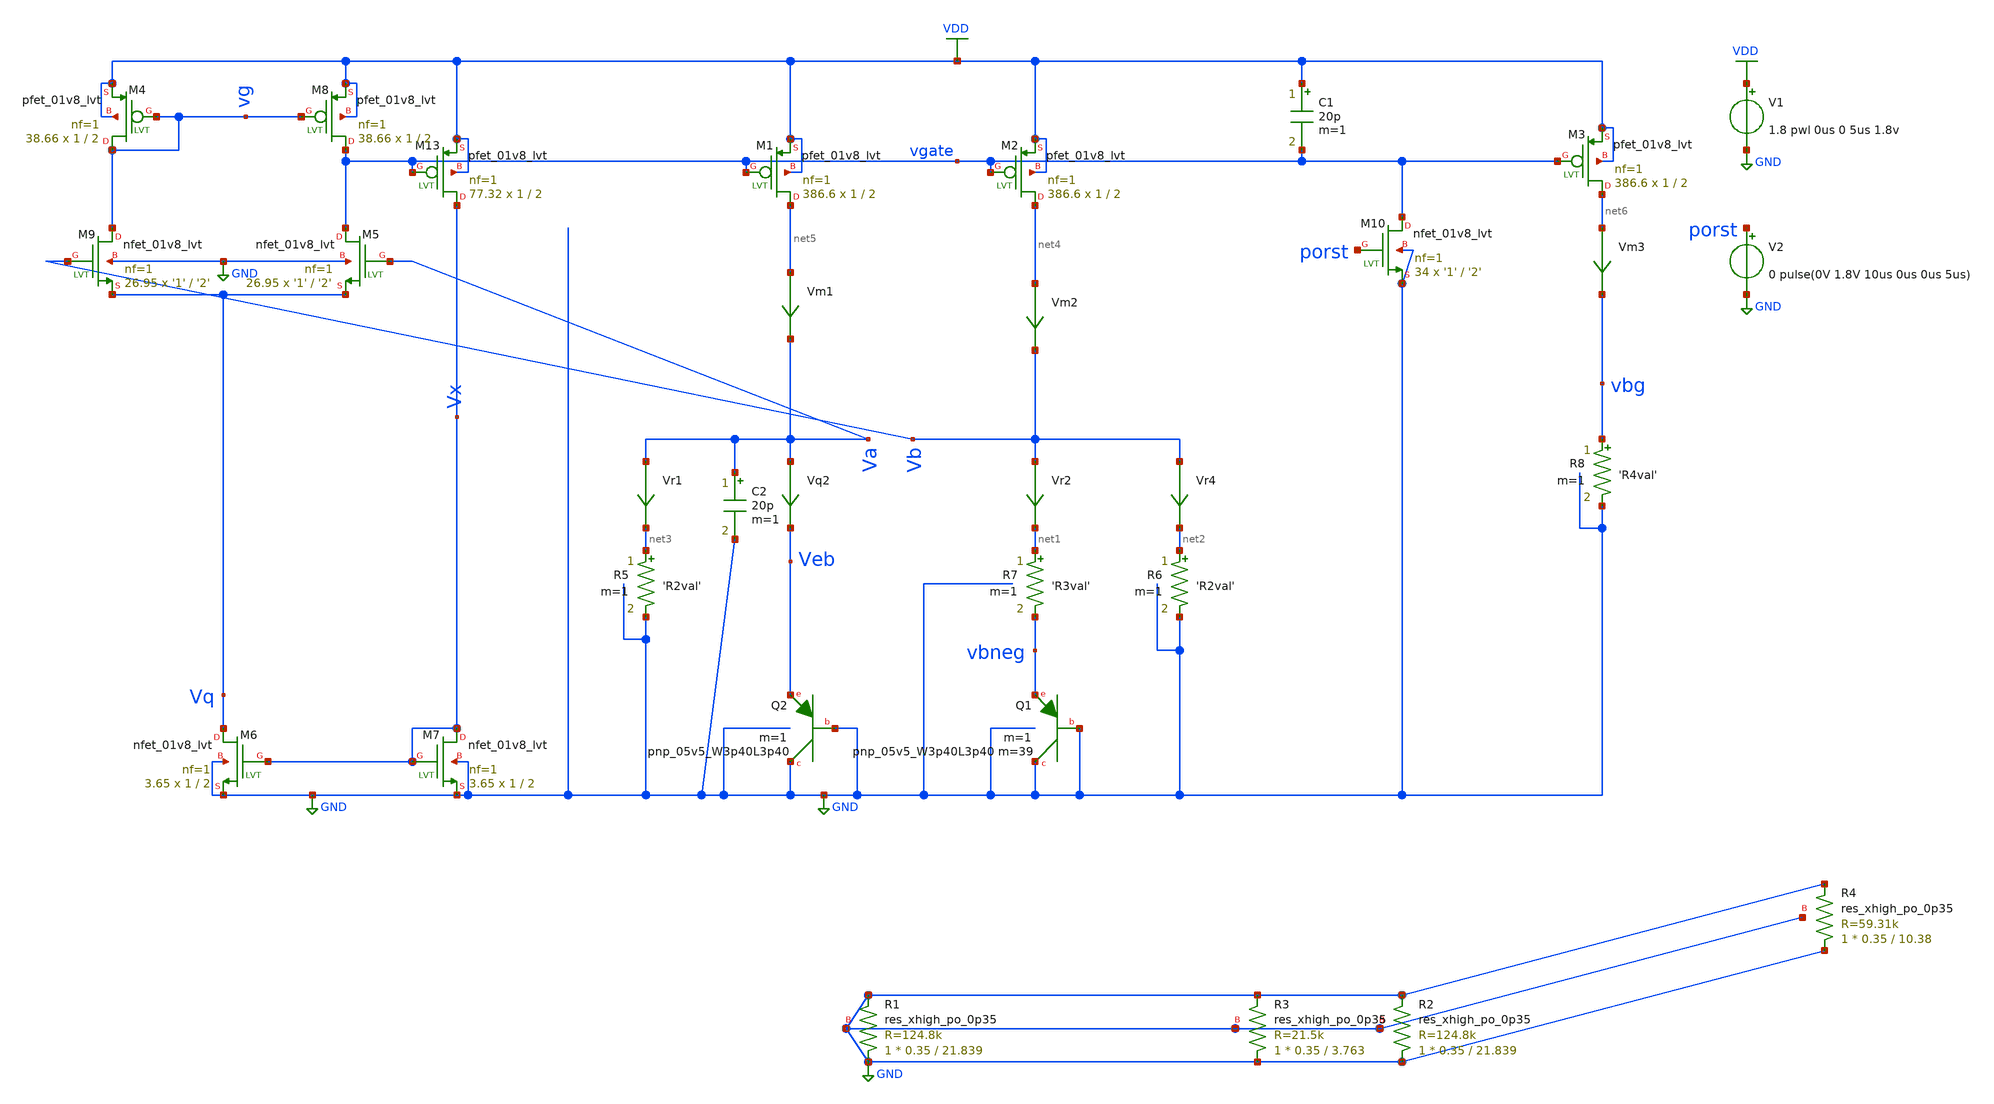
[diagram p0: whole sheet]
** sch_path: schematics/tsmc_bandgap_real.sch
**.subckt tsmc_bandgap_real
V1 VDD GND 1.8 pwl 0us 0 5us 1.8v
XQ2 GND GND Veb sky130_fd_pr__pnp_05v5_W3p40L3p40 m=1
Vr4 Vb net2 0
.save i(vr4)
Vr2 Vb net1 0
.save i(vr2)
Vm1 net5 Va 0
.save i(vm1)
Vm2 net4 Vb 0
.save i(vm2)
Vm3 net6 vbg 0
.save i(vm3)
Vr1 Va net3 0
.save i(vr1)
Vq2 Va Veb 0
.save i(vq2)
XQ1 GND GND vbneg sky130_fd_pr__pnp_05v5_W3p40L3p40 m=39 m=1
XM5 vgate Va Vq GND sky130_fd_pr__nfet_01v8_lvt L='2' W='1' nf=1 ad='int((nf+1)/2) * W/nf * 0.29' as='int((nf+2)/2) * W/nf * 0.29'
+ pd='2*int((nf+1)/2) * (W/nf + 0.29)' ps='2*int((nf+2)/2) * (W/nf + 0.29)' nrd='0.29 / W' nrs='0.29 / W'
+ sa=0 sb=0 sd=0 mult=26.95 m=26.95
XM6 Vq Vx GND GND sky130_fd_pr__nfet_01v8_lvt L=2 W=1 nf=1 ad='int((nf+1)/2) * W/nf * 0.29' as='int((nf+2)/2) * W/nf * 0.29'
+ pd='2*int((nf+1)/2) * (W/nf + 0.29)' ps='2*int((nf+2)/2) * (W/nf + 0.29)' nrd='0.29 / W' nrs='0.29 / W'
+ sa=0 sb=0 sd=0 mult=3.65 m=3.65
XM9 vg Vb Vq GND sky130_fd_pr__nfet_01v8_lvt L='2' W='1' nf=1 ad='int((nf+1)/2) * W/nf * 0.29' as='int((nf+2)/2) * W/nf * 0.29'
+ pd='2*int((nf+1)/2) * (W/nf + 0.29)' ps='2*int((nf+2)/2) * (W/nf + 0.29)' nrd='0.29 / W' nrs='0.29 / W'
+ sa=0 sb=0 sd=0 mult=26.95 m=26.95
XM7 Vx Vx GND GND sky130_fd_pr__nfet_01v8_lvt L=2 W=1 nf=1 ad='int((nf+1)/2) * W/nf * 0.29' as='int((nf+2)/2) * W/nf * 0.29'
+ pd='2*int((nf+1)/2) * (W/nf + 0.29)' ps='2*int((nf+2)/2) * (W/nf + 0.29)' nrd='0.29 / W' nrs='0.29 / W'
+ sa=0 sb=0 sd=0 mult=3.65 m=3.65
XM13 Vx vgate VDD VDD sky130_fd_pr__pfet_01v8_lvt L=2 W=1 nf=1 ad='int((nf+1)/2) * W/nf * 0.29' as='int((nf+2)/2) * W/nf * 0.29'
+ pd='2*int((nf+1)/2) * (W/nf + 0.29)' ps='2*int((nf+2)/2) * (W/nf + 0.29)' nrd='0.29 / W' nrs='0.29 / W'
+ sa=0 sb=0 sd=0 mult=77.32 m=77.32
XM1 net5 vgate VDD VDD sky130_fd_pr__pfet_01v8_lvt L=2 W=1 nf=1 ad='int((nf+1)/2) * W/nf * 0.29' as='int((nf+2)/2) * W/nf * 0.29'
+ pd='2*int((nf+1)/2) * (W/nf + 0.29)' ps='2*int((nf+2)/2) * (W/nf + 0.29)' nrd='0.29 / W' nrs='0.29 / W'
+ sa=0 sb=0 sd=0 mult=386.6 m=386.6
XM2 net4 vgate VDD VDD sky130_fd_pr__pfet_01v8_lvt L=2 W=1 nf=1 ad='int((nf+1)/2) * W/nf * 0.29' as='int((nf+2)/2) * W/nf * 0.29'
+ pd='2*int((nf+1)/2) * (W/nf + 0.29)' ps='2*int((nf+2)/2) * (W/nf + 0.29)' nrd='0.29 / W' nrs='0.29 / W'
+ sa=0 sb=0 sd=0 mult=386.6 m=386.6
XM3 net6 vgate VDD VDD sky130_fd_pr__pfet_01v8_lvt L=2 W=1 nf=1 ad='int((nf+1)/2) * W/nf * 0.29' as='int((nf+2)/2) * W/nf * 0.29'
+ pd='2*int((nf+1)/2) * (W/nf + 0.29)' ps='2*int((nf+2)/2) * (W/nf + 0.29)' nrd='0.29 / W' nrs='0.29 / W'
+ sa=0 sb=0 sd=0 mult=386.6 m=386.6
XR1 GND GND GND sky130_fd_pr__res_xhigh_po_0p35 L=21.839 mult=1 m=1
XR2 GND GND GND sky130_fd_pr__res_xhigh_po_0p35 L=21.839 mult=1 m=1
XR3 GND GND GND sky130_fd_pr__res_xhigh_po_0p35 L=3.763 mult=1 m=1
XR4 GND GND GND sky130_fd_pr__res_xhigh_po_0p35 L=10.38 mult=1 m=1
R7 net1 vbneg 'R3val' m=1
R5 net3 GND 'R2val' m=1
R6 net2 GND 'R2val' m=1
R8 vbg GND 'R4val' m=1
XM4 vg vg VDD VDD sky130_fd_pr__pfet_01v8_lvt L=2 W=1 nf=1 ad='int((nf+1)/2) * W/nf * 0.29' as='int((nf+2)/2) * W/nf * 0.29'
+ pd='2*int((nf+1)/2) * (W/nf + 0.29)' ps='2*int((nf+2)/2) * (W/nf + 0.29)' nrd='0.29 / W' nrs='0.29 / W'
+ sa=0 sb=0 sd=0 mult=38.66 m=38.66
XM8 vgate vg VDD VDD sky130_fd_pr__pfet_01v8_lvt L=2 W=1 nf=1 ad='int((nf+1)/2) * W/nf * 0.29' as='int((nf+2)/2) * W/nf * 0.29'
+ pd='2*int((nf+1)/2) * (W/nf + 0.29)' ps='2*int((nf+2)/2) * (W/nf + 0.29)' nrd='0.29 / W' nrs='0.29 / W'
+ sa=0 sb=0 sd=0 mult=38.66 m=38.66
XM10 vgate porst GND GND sky130_fd_pr__nfet_01v8_lvt L='2' W='1' nf=1 ad='int((nf+1)/2) * W/nf * 0.29'
+ as='int((nf+2)/2) * W/nf * 0.29' pd='2*int((nf+1)/2) * (W/nf + 0.29)' ps='2*int((nf+2)/2) * (W/nf + 0.29)'
+ nrd='0.29 / W' nrs='0.29 / W' sa=0 sb=0 sd=0 mult=34 m=34
V2 porst GND 0 pulse(0V 1.8V 10us 0us 0us 5us)
C1 VDD vgate 20p m=1
C2 Va GND 20p m=1
**** begin user architecture code

.include $::SKYWATER_MODELS/cells/nfet_01v8/sky130_fd_pr__nfet_01v8__tt.corner.spice
.include $::SKYWATER_MODELS/cells/nfet_01v8_lvt/sky130_fd_pr__nfet_01v8_lvt__tt.corner.spice
.include $::SKYWATER_MODELS/cells/pfet_01v8/sky130_fd_pr__pfet_01v8__tt.corner.spice
.include $::SKYWATER_MODELS/cells/nfet_03v3_nvt/sky130_fd_pr__nfet_03v3_nvt__tt.corner.spice
.include $::SKYWATER_MODELS/cells/nfet_05v0_nvt/sky130_fd_pr__nfet_05v0_nvt__tt.corner.spice
.include $::SKYWATER_MODELS/cells/esd_nfet_01v8/sky130_fd_pr__esd_nfet_01v8__tt.corner.spice
.include $::SKYWATER_MODELS/cells/pfet_01v8_lvt/sky130_fd_pr__pfet_01v8_lvt__tt.corner.spice
.include $::SKYWATER_MODELS/cells/pfet_01v8_hvt/sky130_fd_pr__pfet_01v8_hvt__tt.corner.spice
.include $::SKYWATER_MODELS/cells/esd_pfet_g5v0d10v5/sky130_fd_pr__esd_pfet_g5v0d10v5__tt.corner.spice
.include $::SKYWATER_MODELS/cells/pfet_g5v0d10v5/sky130_fd_pr__pfet_g5v0d10v5__tt.corner.spice
.include $::SKYWATER_MODELS/cells/pfet_g5v0d16v0/sky130_fd_pr__pfet_g5v0d16v0__tt.corner.spice
.include $::SKYWATER_MODELS/cells/nfet_g5v0d10v5/sky130_fd_pr__nfet_g5v0d10v5__tt.corner.spice
.include $::SKYWATER_MODELS/cells/nfet_g5v0d16v0/sky130_fd_pr__nfet_g5v0d16v0__tt_discrete.corner.spice
.include $::SKYWATER_MODELS/cells/esd_nfet_g5v0d10v5/sky130_fd_pr__esd_nfet_g5v0d10v5__tt.corner.spice
.include $::SKYWATER_MODELS/models/corners/tt/nonfet.spice
* Mismatch parameters
.include $::SKYWATER_MODELS/cells/nfet_01v8/sky130_fd_pr__nfet_01v8__mismatch.corner.spice
.include $::SKYWATER_MODELS/cells/pfet_01v8/sky130_fd_pr__pfet_01v8__mismatch.corner.spice
.include $::SKYWATER_MODELS/cells/nfet_01v8_lvt/sky130_fd_pr__nfet_01v8_lvt__mismatch.corner.spice
.include $::SKYWATER_MODELS/cells/pfet_01v8_lvt/sky130_fd_pr__pfet_01v8_lvt__mismatch.corner.spice
.include $::SKYWATER_MODELS/cells/pfet_01v8_hvt/sky130_fd_pr__pfet_01v8_hvt__mismatch.corner.spice
.include $::SKYWATER_MODELS/cells/nfet_g5v0d10v5/sky130_fd_pr__nfet_g5v0d10v5__mismatch.corner.spice
.include $::SKYWATER_MODELS/cells/pfet_g5v0d10v5/sky130_fd_pr__pfet_g5v0d10v5__mismatch.corner.spice
.include $::SKYWATER_MODELS/cells/nfet_05v0_nvt/sky130_fd_pr__nfet_05v0_nvt__mismatch.corner.spice
.include $::SKYWATER_MODELS/cells/nfet_03v3_nvt/sky130_fd_pr__nfet_03v3_nvt__mismatch.corner.spice
* Resistor$::SKYWATER_MODELS/Capacitor
.include $::SKYWATER_MODELS/models/r+c/res_typical__cap_typical.spice
.include $::SKYWATER_MODELS/models/r+c/res_typical__cap_typical__lin.spice
* Special cells
.include $::SKYWATER_MODELS/models/corners/tt/specialized_cells.spice
* All models
.include $::SKYWATER_MODELS/models/all.spice
.include $::SKYWATER_MODELS/cells/pnp_05v5/sky130_fd_pr__pnp_05v5_W3p40L3p40.model.spice
* Corner
.include $::SKYWATER_MODELS/models/corners/tt/rf.spice



.option savecurrents
.param R3val='22.187k'
.param alpha='1'
.param R2R3ratio='5.6555038*alpha'
.param R2val='R3val*R2R3ratio'
.param R4R2ratio='0.47810041'
.param R4val='R2val*R4R2ratio
.nodeset v(vgate)=1.3
.option temp=27
.control
save all  @m.xm1.msky130_fd_pr__pfet_01v8_lvt[gm]  @m.xm2.msky130_fd_pr__pfet_01v8_lvt[gm]  @m.xm3.msky130_fd_pr__pfet_01v8_lvt[gm]  @m.xm4.msky130_fd_pr__pfet_01v8_lvt[gm]  @m.xm5.msky130_fd_pr__nfet_01v8_lvt[gm]  @m.xm6.msky130_fd_pr__nfet_01v8_lvt[gm]  @m.xm7.msky130_fd_pr__nfet_01v8_lvt[gm]  @m.xm8.msky130_fd_pr__pfet_01v8_lvt[gm]  @m.xm9.msky130_fd_pr__nfet_01v8_lvt[gm]  @m.xm13.msky130_fd_pr__pfet_01v8_lvt[gm]

op
write tsmc_bandgap_real.raw
let id8=@m.xm8.msky130_fd_pr__pfet_01v8_lvt[id]
let id1=@m.xm1.msky130_fd_pr__pfet_01v8_lvt[id]
let vth5=@m.xm5.msky130_fd_pr__nfet_01v8_lvt[vth]
let vth6=@m.xm6.msky130_fd_pr__nfet_01v8_lvt[vth]
let wm8=@m.xm8.msky130_fd_pr__pfet_01v8_lvt[w]
let mm8=@m.xm8.msky130_fd_pr__pfet_01v8_lvt[m]
let weff8=wm8*mm8
let jd8=id8/weff8
let wm1=@m.xm1.msky130_fd_pr__pfet_01v8_lvt[w]
let mm1=@m.xm1.msky130_fd_pr__pfet_01v8_lvt[m]
let weff1=wm1*mm1
let jd1=id1/weff1
let wm13=@m.xm13.msky130_fd_pr__pfet_01v8_lvt[w]
let mm13=@m.xm13.msky130_fd_pr__pfet_01v8_lvt[m]
let weff13=wm13*mm13
let id13=@m.xm13.msky130_fd_pr__pfet_01v8_lvt[id]
let jd13=id13/weff13
let gm13=@m.xm13.msky130_fd_pr__pfet_01v8_lvt[gm]
let gm3=@m.xm3.msky130_fd_pr__pfet_01v8_lvt[gm]
let gm4=@m.xm4.msky130_fd_pr__pfet_01v8_lvt[gm]
let gm5=@m.xm5.msky130_fd_pr__nfet_01v8_lvt[gm]
let gm6=@m.xm6.msky130_fd_pr__nfet_01v8_lvt[gm]
let gm7=@m.xm7.msky130_fd_pr__nfet_01v8_lvt[gm]
let gm8=@m.xm8.msky130_fd_pr__pfet_01v8_lvt[gm]
let gm9=@m.xm9.msky130_fd_pr__nfet_01v8_lvt[gm]
let gm1=@m.xm1.msky130_fd_pr__pfet_01v8_lvt[gm]
let gm2=@m.xm2.msky130_fd_pr__pfet_01v8_lvt[gm]
let vdsat1=2/(gm1/vm1#branch)
let vdsat2=2/(gm2/vm2#branch)
let vdsat3=2/(gm3/vm3#branch)
let vdsat4=2/(gm4/@m.xm4.msky130_fd_pr__pfet_01v8_lvt[id])
let vdsat5=2/(gm5/@m.xm5.msky130_fd_pr__nfet_01v8_lvt[id])
let vdsat6=2/(gm6/@m.xm6.msky130_fd_pr__nfet_01v8_lvt[id])
let vdsat7=2/(gm7/@m.xm7.msky130_fd_pr__nfet_01v8_lvt[id])
let vdsat8=2/(gm8/@m.xm8.msky130_fd_pr__pfet_01v8_lvt[id])
let vdsat9=2/(gm9/@m.xm9.msky130_fd_pr__nfet_01v8_lvt[id])
let vdsat13=2/(gm13/@m.xm13.msky130_fd_pr__pfet_01v8_lvt[id])


print vbg vgate vg va vb vx vq
print vdsat1 vdsat2 vdsat3 vdsat4   vdsat5 vdsat6 vdsat7 vdsat8 vdsat9 vdsat13
.endc


**** end user architecture code
**.ends
.GLOBAL VDD
.GLOBAL GND
.end
